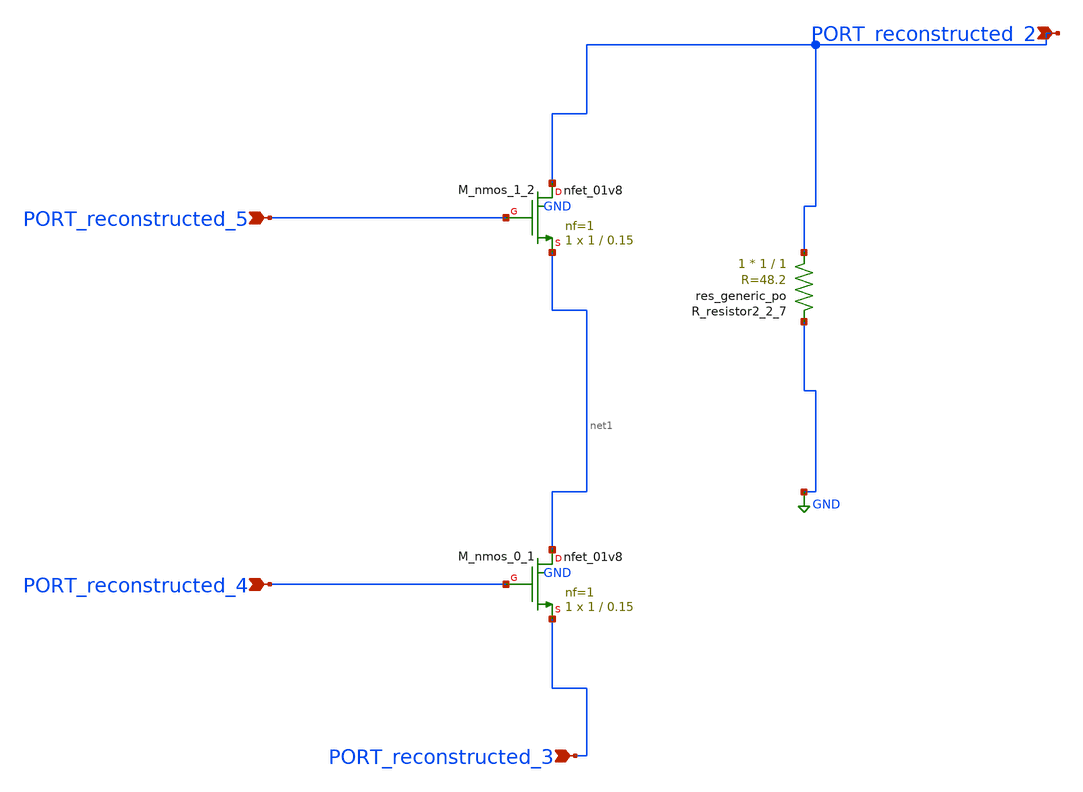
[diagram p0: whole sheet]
** sch_path: schematics/SchemGen/10_37649_AJES-25-014_06_002.sch
**.subckt 10_37649_AJES-25-014_06_002 PORT_reconstructed_3 PORT_reconstructed_4 PORT_reconstructed_5
*+ PORT_reconstructed_2
*.ipin PORT_reconstructed_3
*.ipin PORT_reconstructed_4
*.ipin PORT_reconstructed_5
*.ipin PORT_reconstructed_2
XM_nmos_0_1 net1 PORT_reconstructed_4 PORT_reconstructed_3 GND sky130_fd_pr__nfet_01v8 L=0.15 W=1 nf=1
+ ad='int((1 + 1)/2) * 1 / 1 * 0.29' as='int((1 + 2)/2) * 1 / 1 * 0.29' pd='2*int((1 + 1)/2) * (1 / 1 + 0.29)'
+ ps='2*int((1 + 2)/2) * (1 / 1 + 0.29)' nrd='0.29 / 1 ' nrs='0.29 / 1 ' sa=0 sb=0 sd=0 mult=1 m=1
XM_nmos_1_2 PORT_reconstructed_2 PORT_reconstructed_5 net1 GND sky130_fd_pr__nfet_01v8 L=0.15 W=1 nf=1
+ ad='int((1 + 1)/2) * 1 / 1 * 0.29' as='int((1 + 2)/2) * 1 / 1 * 0.29' pd='2*int((1 + 1)/2) * (1 / 1 + 0.29)'
+ ps='2*int((1 + 2)/2) * (1 / 1 + 0.29)' nrd='0.29 / 1 ' nrs='0.29 / 1 ' sa=0 sb=0 sd=0 mult=1 m=1
XR_resistor2_2_7 PORT_reconstructed_2 GND sky130_fd_pr__res_generic_po W=1 L=1 m=1
**.ends
.GLOBAL GND
.end
